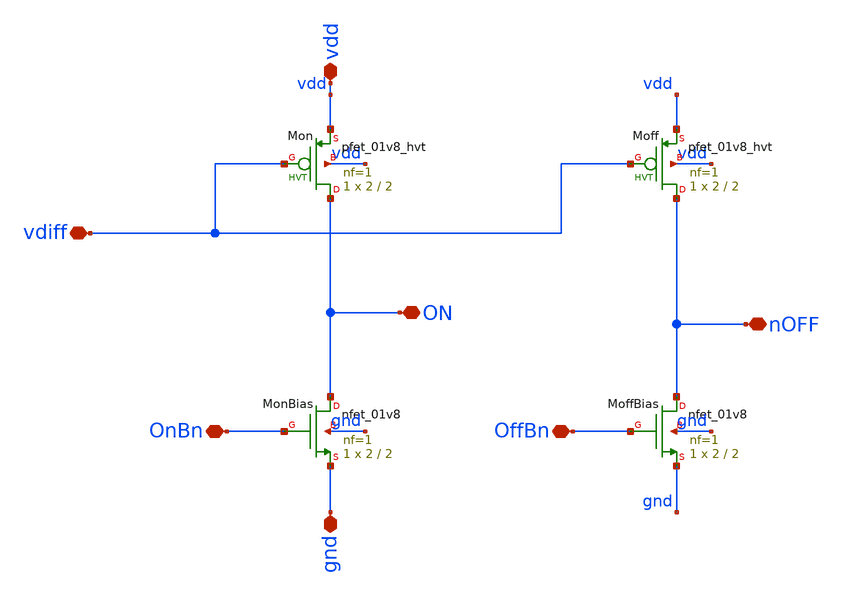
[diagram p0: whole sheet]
** sch_path: analog/xschem/PixelComparators.sch
**.subckt PixelComparators OnBn OffBn vdd vdiff gnd ON nOFF
*.iopin OnBn
*.iopin OffBn
*.iopin vdd
*.iopin vdiff
*.iopin gnd
*.iopin ON
*.iopin nOFF
XMonBias ON OnBn gnd gnd sky130_fd_pr__nfet_01v8 L=2 W=2 nf=1 ad='int((1 + 1)/2) * 2 / 1 * 0.29' as='int((1 + 2)/2) * 2 / 1 * 0.29'
+ pd='2*int((1 + 1)/2) * (2 / 1 + 0.29)' ps='2*int((1 + 2)/2) * (2 / 1 + 0.29)' nrd='0.29 / 2 ' nrs='0.29 / 2 '
+ sa=0 sb=0 sd=0 mult=1 m=1
XMoffBias nOFF OffBn gnd gnd sky130_fd_pr__nfet_01v8 L=2 W=2 nf=1 ad='int((1 + 1)/2) * 2 / 1 * 0.29'
+ as='int((1 + 2)/2) * 2 / 1 * 0.29' pd='2*int((1 + 1)/2) * (2 / 1 + 0.29)' ps='2*int((1 + 2)/2) * (2 / 1 + 0.29)'
+ nrd='0.29 / 2 ' nrs='0.29 / 2 ' sa=0 sb=0 sd=0 mult=1 m=1
XMon ON vdiff vdd vdd sky130_fd_pr__pfet_01v8_hvt L=2 W=2 nf=1 ad='int((1 + 1)/2) * 2 / 1 * 0.29' as='int((1 + 2)/2) * 2 / 1 * 0.29'
+ pd='2*int((1 + 1)/2) * (2 / 1 + 0.29)' ps='2*int((1 + 2)/2) * (2 / 1 + 0.29)' nrd='0.29 / 2 ' nrs='0.29 / 2 '
+ sa=0 sb=0 sd=0 mult=1 m=1
XMoff nOFF vdiff vdd vdd sky130_fd_pr__pfet_01v8_hvt L=2 W=2 nf=1 ad='int((1 + 1)/2) * 2 / 1 * 0.29'
+ as='int((1 + 2)/2) * 2 / 1 * 0.29' pd='2*int((1 + 1)/2) * (2 / 1 + 0.29)' ps='2*int((1 + 2)/2) * (2 / 1 + 0.29)'
+ nrd='0.29 / 2 ' nrs='0.29 / 2 ' sa=0 sb=0 sd=0 mult=1 m=1
**.ends
.end
